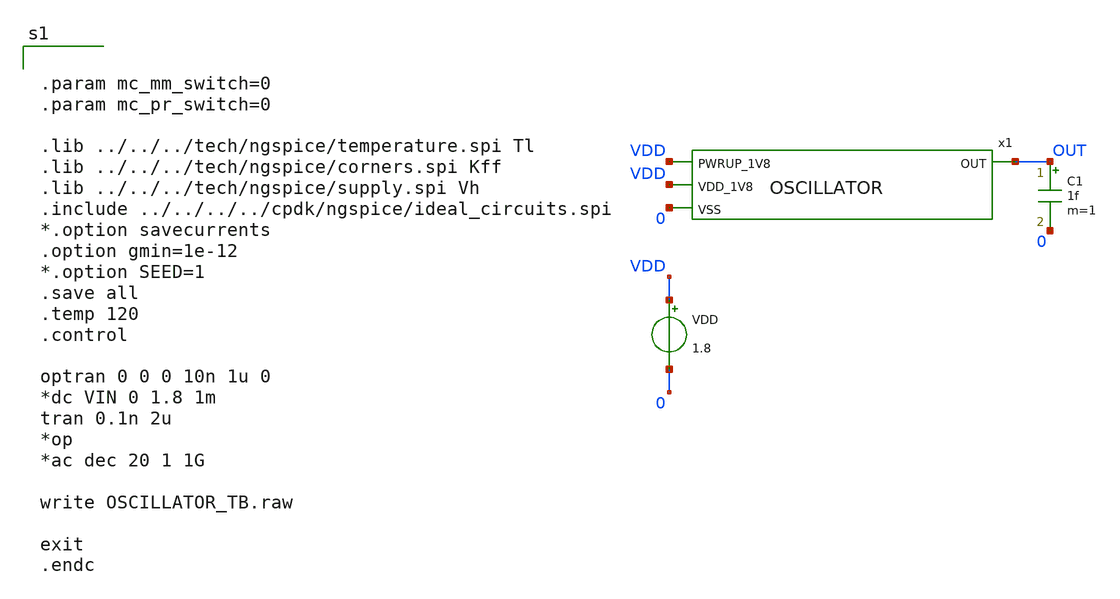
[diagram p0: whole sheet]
** sch_path: design/LELO_GR03_SKY130A/OSCILLATOR_TB_xsch.sch
**.subckt OSCILLATOR_TB_xsch
x1 VDD OUT VDD 0 OSCILLATOR
VDD VDD 0 1.8
C1 OUT 0 1f m=1
**** begin user architecture code


.param mc_mm_switch=0
.param mc_pr_switch=0

.lib ../../../tech/ngspice/temperature.spi Tl
.lib ../../../tech/ngspice/corners.spi Kff
.lib ../../../tech/ngspice/supply.spi Vh
.include ../../../../cpdk/ngspice/ideal_circuits.spi
*.option savecurrents
.option gmin=1e-12
*.option SEED=1
.save all
.temp 120
.control

optran 0 0 0 10n 1u 0
*dc VIN 0 1.8 1m
tran 0.1n 2u
*op
*ac dec 20 1 1G

write OSCILLATOR_TB.raw

exit
.endc


**** end user architecture code
**.ends
.end
